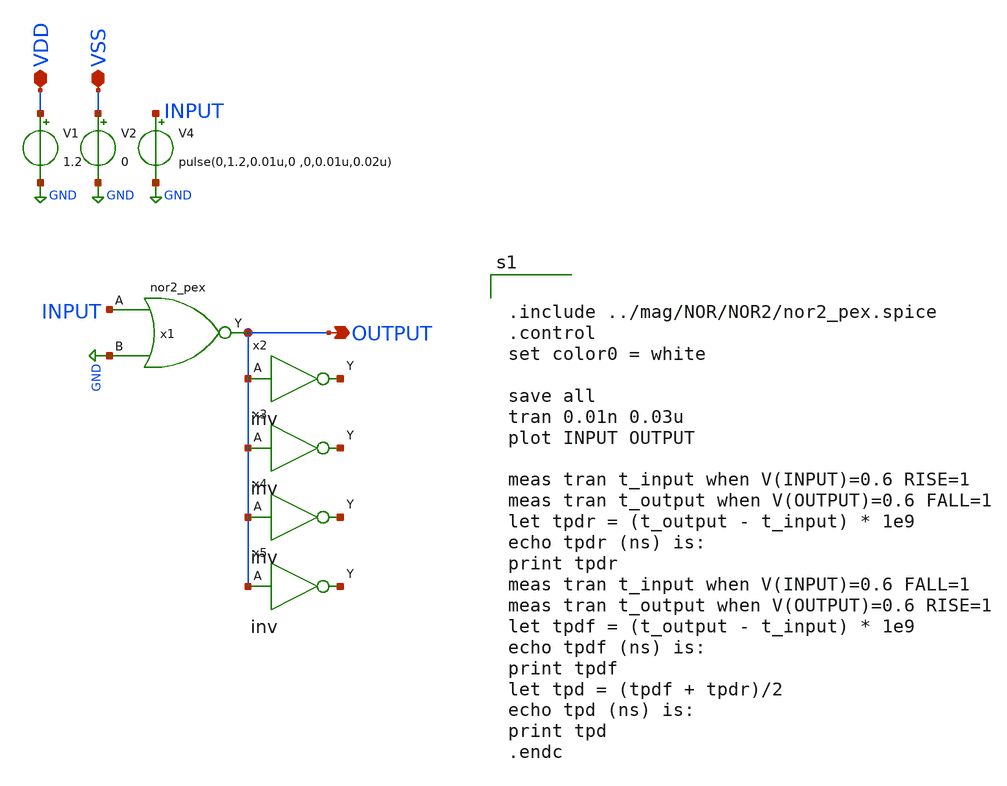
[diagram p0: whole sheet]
** sch_path: design/xschem/NOR/nor2_TB_magic.sch
**.subckt nor2_TB_magic OUTPUT VDD VSS
*.opin OUTPUT
*.iopin VDD
*.iopin VSS
V1 VDD GND 1.2
V2 VSS GND 0
V4 INPUT GND pulse(0,1.2,0.01u,0 ,0,0.01u,0.02u)
x2 OUTPUT VSS VDD net1 inv
x3 OUTPUT VSS VDD net2 inv
x4 OUTPUT VSS VDD net3 inv
x5 OUTPUT VSS VDD net4 inv
x1 INPUT GND VSS VDD OUTPUT nor2_pex
**** begin user architecture code

** opencircuitdesign pdks install
.lib $::SKYWATER_MODELS/sky130.lib.spice tt_mm




.include ../mag/NOR/NOR2/nor2_pex.spice
.control
set color0 = white

save all
tran 0.01n 0.03u
plot INPUT OUTPUT

meas tran t_input when V(INPUT)=0.6 RISE=1
meas tran t_output when V(OUTPUT)=0.6 FALL=1
let tpdr = (t_output - t_input) * 1e9
echo tpdr (ns) is:
print tpdr
meas tran t_input when V(INPUT)=0.6 FALL=1
meas tran t_output when V(OUTPUT)=0.6 RISE=1
let tpdf = (t_output - t_input) * 1e9
echo tpdf (ns) is:
print tpdf
let tpd = (tpdf + tpdr)/2
echo tpd (ns) is:
print tpd
.endc


**** end user architecture code
**.ends

* expanding   symbol:  INV/inv.sym # of pins=2
** sym_path: design/xschem/INV/inv.sym
** sch_path: design/xschem/INV/inv.sch
.subckt inv A VSS VDD Y
*.ipin A
*.opin Y
XM2 Y A VSS GND sky130_fd_pr__nfet_01v8 L=0.15 W=1 nf=1 ad='int((nf+1)/2) * W/nf * 0.29' as='int((nf+2)/2) * W/nf * 0.29'
+ pd='2*int((nf+1)/2) * (W/nf + 0.29)' ps='2*int((nf+2)/2) * (W/nf + 0.29)' nrd='0.29 / W' nrs='0.29 / W'
+ sa=0 sb=0 sd=0 mult=1 m=1
XM1 Y A VDD VDD sky130_fd_pr__pfet_01v8 L=0.15 W=3.21 nf=1 ad='int((nf+1)/2) * W/nf * 0.29' as='int((nf+2)/2) * W/nf * 0.29'
+ pd='2*int((nf+1)/2) * (W/nf + 0.29)' ps='2*int((nf+2)/2) * (W/nf + 0.29)' nrd='0.29 / W' nrs='0.29 / W'
+ sa=0 sb=0 sd=0 mult=1 m=1
.ends

.GLOBAL GND
.end
